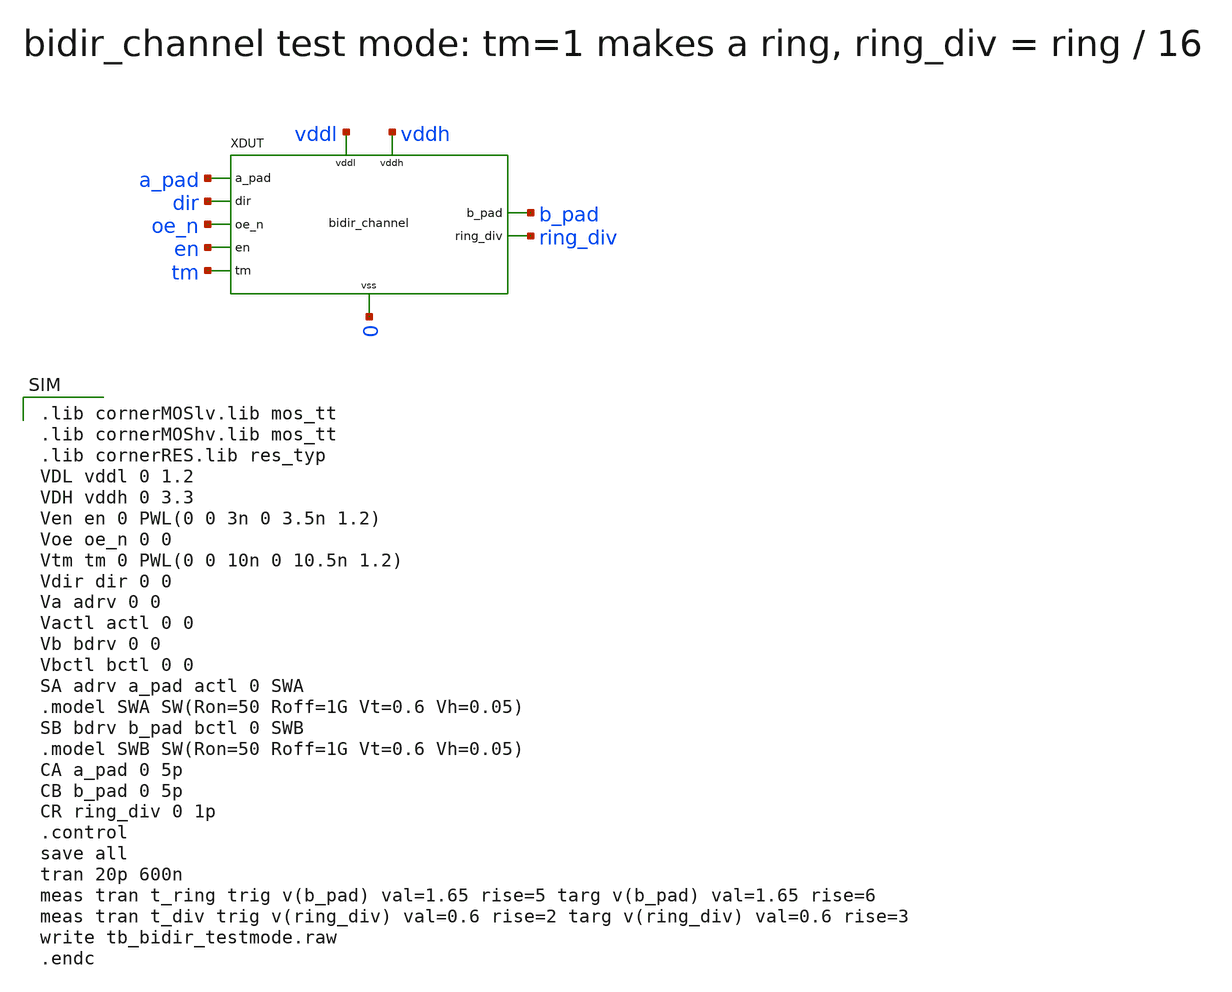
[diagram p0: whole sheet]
** sch_path: verification/tb_bidir_testmode.sch
**.subckt tb_bidir_testmode
XDUT a_pad b_pad dir oe_n en tm ring_div vddl vddh 0 bidir_channel
**** begin user architecture code

.lib cornerMOSlv.lib mos_tt
.lib cornerMOShv.lib mos_tt
.lib cornerRES.lib res_typ
VDL vddl 0 1.2
VDH vddh 0 3.3
Ven en 0 PWL(0 0 3n 0 3.5n 1.2)
Voe oe_n 0 0
Vtm tm 0 PWL(0 0 10n 0 10.5n 1.2)
Vdir dir 0 0
Va adrv 0 0
Vactl actl 0 0
Vb bdrv 0 0
Vbctl bctl 0 0
SA adrv a_pad actl 0 SWA
.model SWA SW(Ron=50 Roff=1G Vt=0.6 Vh=0.05)
SB bdrv b_pad bctl 0 SWB
.model SWB SW(Ron=50 Roff=1G Vt=0.6 Vh=0.05)
CA a_pad 0 5p
CB b_pad 0 5p
CR ring_div 0 1p
.control
save all
tran 20p 600n
meas tran t_ring trig v(b_pad) val=1.65 rise=5 targ v(b_pad) val=1.65 rise=6
meas tran t_div trig v(ring_div) val=0.6 rise=2 targ v(ring_div) val=0.6 rise=3
write tb_bidir_testmode.raw
.endc

**** end user architecture code
**.ends
.end
